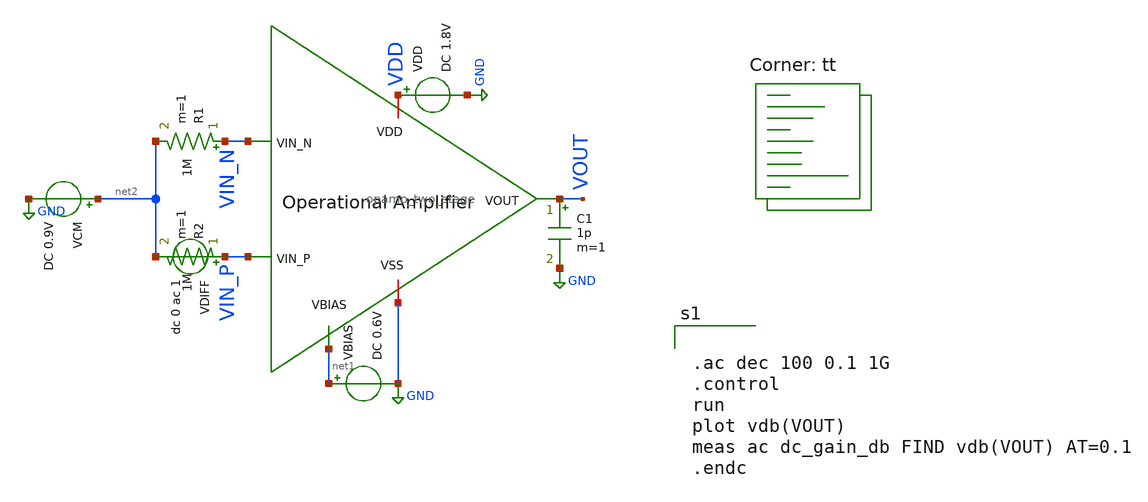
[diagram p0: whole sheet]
** sch_path: analog/bootcamp_opamp/build/schematic/tb_ac_analysis.sch
**.subckt tb_ac_analysis
x1 VDD VOUT VIN_N VIN_P net1 GND opamp_two_stage
VCM net2 GND DC 0.9V
VDD VDD GND DC 1.8V
VBIAS net1 GND DC 0.6V
C1 VOUT GND 1p m=1
VDIFF VIN_P net2 dc 0 ac 1
R1 VIN_N net2 1M m=1
R2 VIN_P net2 1M m=1
**** begin user architecture code


.ac dec 100 0.1 1G
.control
run
plot vdb(VOUT)
meas ac dc_gain_db FIND vdb(VOUT) AT=0.1
.endc


.lib $::SKYWATER_MODELS/sky130.lib.spice tt
**** end user architecture code
**.ends

* expanding   symbol:  opamp_two_stage.sym # of pins=6
** sym_path: analog/bootcamp_opamp/build/schematic/opamp_two_stage.sym
** sch_path: analog/bootcamp_opamp/build/schematic/opamp_two_stage.sch
.subckt opamp_two_stage VDD VOUT VIN_N VIN_P VBIAS VSS
*.ipin VIN_P
*.ipin VIN_N
*.iopin VDD
*.iopin VSS
*.ipin VBIAS
*.opin VOUT
XM1 net2 VIN_N net1 VSS sky130_fd_pr__nfet_01v8 L=0.500 W=0.420 nf=1 ad='int((nf+1)/2) * W/nf * 0.29'
+ as='int((nf+2)/2) * W/nf * 0.29' pd='2*int((nf+1)/2) * (W/nf + 0.29)' ps='2*int((nf+2)/2) * (W/nf + 0.29)'
+ nrd='0.29 / W' nrs='0.29 / W' sa=0 sb=0 sd=0 mult=1 m=1
XM2 net3 VIN_P net1 VSS sky130_fd_pr__nfet_01v8 L=0.500 W=0.420 nf=1 ad='int((nf+1)/2) * W/nf * 0.29'
+ as='int((nf+2)/2) * W/nf * 0.29' pd='2*int((nf+1)/2) * (W/nf + 0.29)' ps='2*int((nf+2)/2) * (W/nf + 0.29)'
+ nrd='0.29 / W' nrs='0.29 / W' sa=0 sb=0 sd=0 mult=1 m=1
XM3 net2 net2 VDD VDD sky130_fd_pr__pfet_01v8 L=1.000 W=0.893 nf=1 ad='int((nf+1)/2) * W/nf * 0.29' as='int((nf+2)/2) * W/nf * 0.29'
+ pd='2*int((nf+1)/2) * (W/nf + 0.29)' ps='2*int((nf+2)/2) * (W/nf + 0.29)' nrd='0.29 / W' nrs='0.29 / W'
+ sa=0 sb=0 sd=0 mult=1 m=1
XM4 net3 net2 VDD VDD sky130_fd_pr__pfet_01v8 L=1.000 W=0.893 nf=1 ad='int((nf+1)/2) * W/nf * 0.29' as='int((nf+2)/2) * W/nf * 0.29'
+ pd='2*int((nf+1)/2) * (W/nf + 0.29)' ps='2*int((nf+2)/2) * (W/nf + 0.29)' nrd='0.29 / W' nrs='0.29 / W'
+ sa=0 sb=0 sd=0 mult=1 m=1
XM5 net1 VBIAS VSS VSS sky130_fd_pr__nfet_01v8 L=1.000 W=0.463 nf=1 ad='int((nf+1)/2) * W/nf * 0.29'
+ as='int((nf+2)/2) * W/nf * 0.29' pd='2*int((nf+1)/2) * (W/nf + 0.29)' ps='2*int((nf+2)/2) * (W/nf + 0.29)'
+ nrd='0.29 / W' nrs='0.29 / W' sa=0 sb=0 sd=0 mult=1 m=1
XM6 VOUT net3 VDD VDD sky130_fd_pr__pfet_01v8 L=0.500 W=52.380 nf=1 ad='int((nf+1)/2) * W/nf * 0.29'
+ as='int((nf+2)/2) * W/nf * 0.29' pd='2*int((nf+1)/2) * (W/nf + 0.29)' ps='2*int((nf+2)/2) * (W/nf + 0.29)'
+ nrd='0.29 / W' nrs='0.29 / W' sa=0 sb=0 sd=0 mult=1 m=1
XC1 VOUT net3 sky130_fd_pr__cap_mim_m3_1 W=10 L=12.5 MF=1 m=1
XM7 VOUT VBIAS VSS VSS sky130_fd_pr__nfet_01v8 L=1.000 W=48.290 nf=1 ad='int((nf+1)/2) * W/nf * 0.29'
+ as='int((nf+2)/2) * W/nf * 0.29' pd='2*int((nf+1)/2) * (W/nf + 0.29)' ps='2*int((nf+2)/2) * (W/nf + 0.29)'
+ nrd='0.29 / W' nrs='0.29 / W' sa=0 sb=0 sd=0 mult=1 m=1
.ends

.GLOBAL GND
.GLOBAL VDD
.GLOBAL VSS
.end
